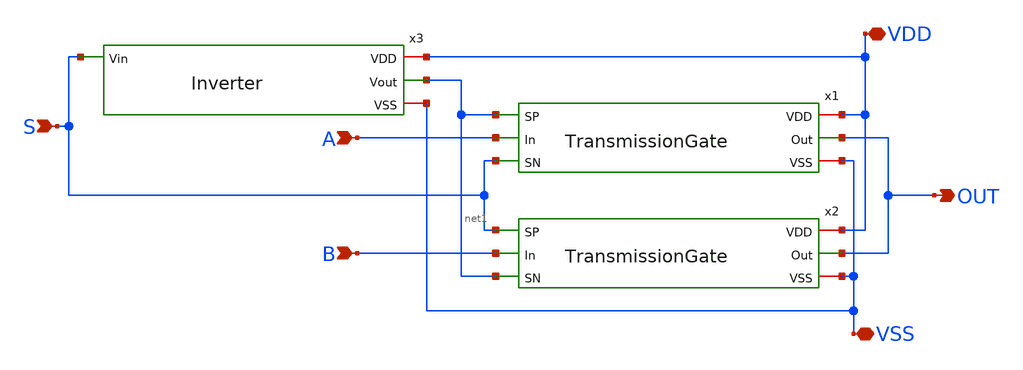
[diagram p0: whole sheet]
** sch_path: xschem/2-1MUX.sch
**.subckt 2-1MUX A B S VDD VSS OUT
*.ipin A
*.ipin B
*.ipin S
*.iopin VDD
*.iopin VSS
*.opin OUT
x1 net1 VDD OUT A VSS S TransmissionGate
x2 S VDD OUT B VSS net1 TransmissionGate
x3 VDD S net1 VSS Inverter
**.ends

* expanding   symbol:  TransmissionGate.sym # of pins=6
** sym_path: xschem/TransmissionGate.sym
** sch_path: xschem/TransmissionGate.sch
.subckt TransmissionGate SP VDD Out In VSS SN
*.opin Out
*.ipin In
*.ipin SP
*.iopin VDD
*.iopin VSS
*.ipin SN
XM1 In SN Out VSS sky130_fd_pr__nfet_g5v0d10v5 L=0.5 W=0.75 nf=1 ad='int((nf+1)/2) * W/nf * 0.29' as='int((nf+2)/2) * W/nf * 0.29'
+ pd='2*int((nf+1)/2) * (W/nf + 0.29)' ps='2*int((nf+2)/2) * (W/nf + 0.29)' nrd='0.29 / W' nrs='0.29 / W'
+ sa=0 sb=0 sd=0 mult=1 m=1
XM2 In SP Out VDD sky130_fd_pr__pfet_g5v0d10v5 L=0.5 W=1.5 nf=1 ad='int((nf+1)/2) * W/nf * 0.29' as='int((nf+2)/2) * W/nf * 0.29'
+ pd='2*int((nf+1)/2) * (W/nf + 0.29)' ps='2*int((nf+2)/2) * (W/nf + 0.29)' nrd='0.29 / W' nrs='0.29 / W'
+ sa=0 sb=0 sd=0 mult=1 m=1
.ends


* expanding   symbol:  Inverter.sym # of pins=4
** sym_path: xschem/Inverter.sym
** sch_path: xschem/Inverter.sch
.subckt Inverter VDD Vin Vout VSS
*.ipin Vin
*.iopin VDD
*.iopin VSS
*.opin Vout
XM1 Vout Vin VSS VSS sky130_fd_pr__nfet_g5v0d10v5 L=0.5 W=0.75 nf=1 ad='int((nf+1)/2) * W/nf * 0.29'
+ as='int((nf+2)/2) * W/nf * 0.29' pd='2*int((nf+1)/2) * (W/nf + 0.29)' ps='2*int((nf+2)/2) * (W/nf + 0.29)'
+ nrd='0.29 / W' nrs='0.29 / W' sa=0 sb=0 sd=0 mult=1 m=1
XM2 Vout Vin VDD VDD sky130_fd_pr__pfet_g5v0d10v5 L=0.5 W=1.5 nf=1 ad='int((nf+1)/2) * W/nf * 0.29' as='int((nf+2)/2) * W/nf * 0.29'
+ pd='2*int((nf+1)/2) * (W/nf + 0.29)' ps='2*int((nf+2)/2) * (W/nf + 0.29)' nrd='0.29 / W' nrs='0.29 / W'
+ sa=0 sb=0 sd=0 mult=1 m=1
.ends

.end
